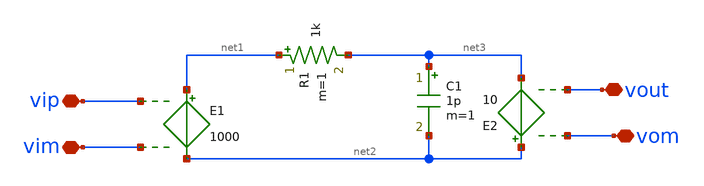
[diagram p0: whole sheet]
** sch_path: xschem/symb_1.sch
**.subckt symb_1 vip vim vout vom
*.iopin vip
*.iopin vim
*.iopin vout
*.iopin vom
E1 net1 net2 vip vim 1000
R1 net1 net3 1k m=1
C1 net3 net2 1p m=1
E2 net2 net3 vom vout 10
**.ends
.end
